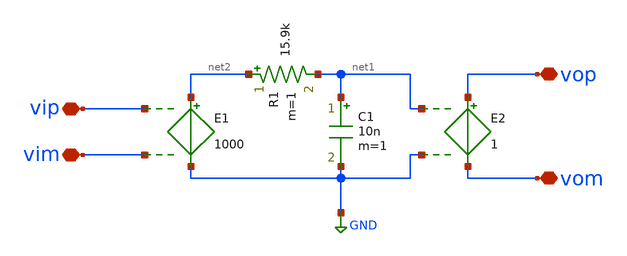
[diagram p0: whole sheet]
** sch_path: work/xschem/buf_Opamp.sch
**.subckt buf_Opamp vop vom vim vip
*.iopin vop
*.iopin vom
*.iopin vim
*.iopin vip
E1 net2 GND vip vim 1000
E2 vop vom net1 GND 1
R1 net2 net1 15.9k m=1
C1 net1 GND 10n m=1
**.ends
.GLOBAL GND
.end
